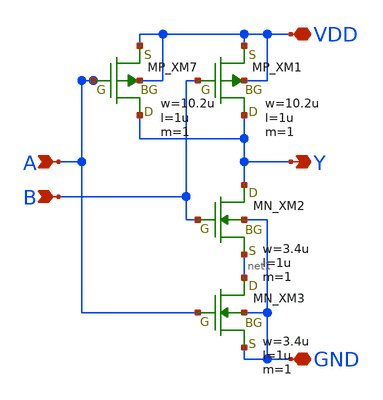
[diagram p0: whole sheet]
** sch_path: openIP62_rev1.0/IP62/Technology/tech/symbols/Xschem/IP62_5_stdcell/NAND2.sch
**.subckt NAND2 B A Y GND VDD
*.ipin B
*.ipin A
*.opin Y
*.iopin GND
*.iopin VDD
XM7 Y A VDD VDD PMOS w=10.2u l=1u as=0 ad=0 ps=0 pd=0 nrd=0 nrs=0 m=1
XM1 Y B VDD VDD PMOS w=10.2u l=1u as=0 ad=0 ps=0 pd=0 nrd=0 nrs=0 m=1
XM2 Y B net1 GND NMOS w=3.4u l=1u as=0 ad=0 ps=0 pd=0 nrd=0 nrs=0 m=1
XM3 net1 A GND GND NMOS w=3.4u l=1u as=0 ad=0 ps=0 pd=0 nrd=0 nrs=0 m=1
**.ends
.end
